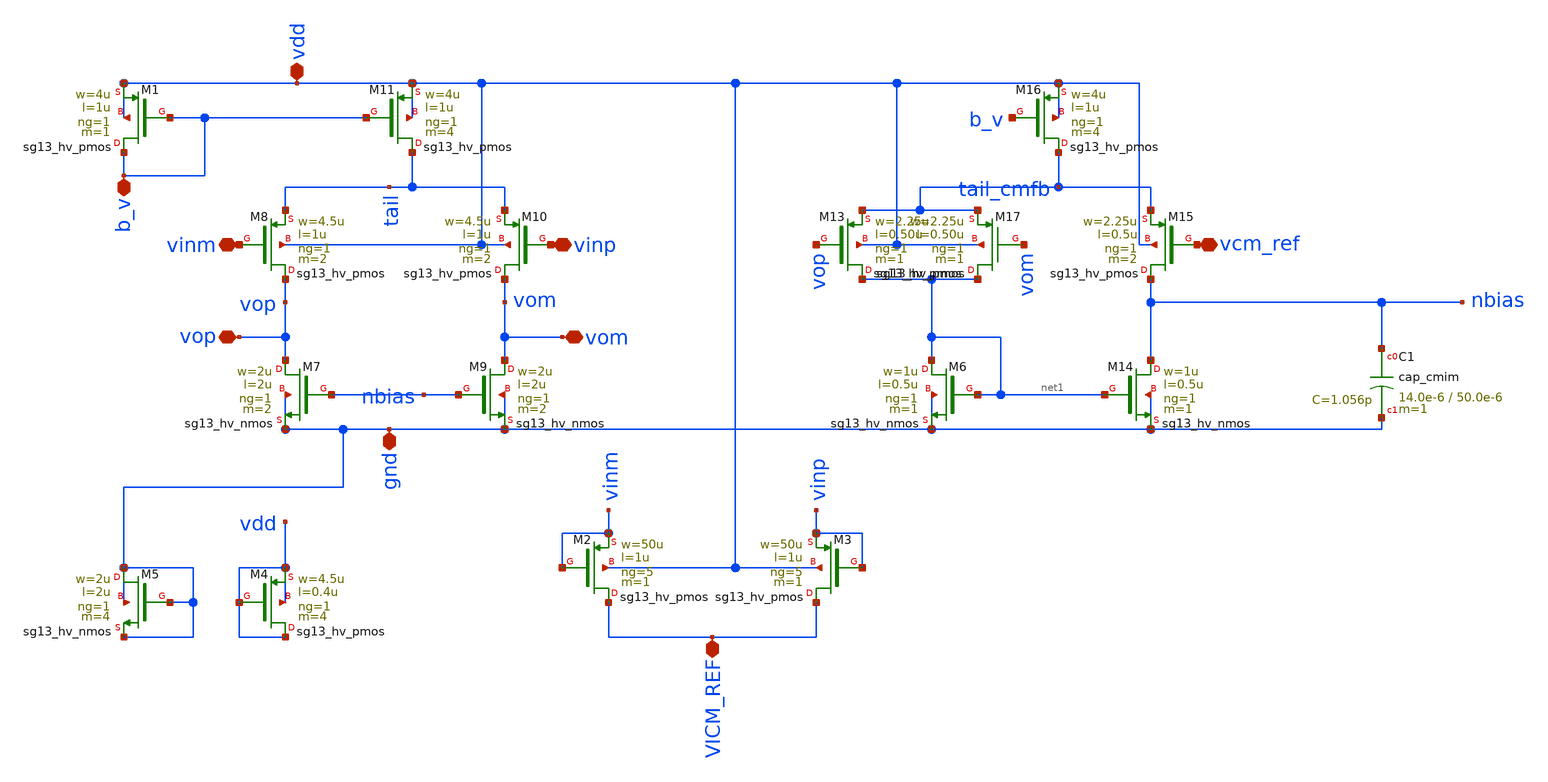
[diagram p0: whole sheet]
** sch_path: dependencies/OTA/OTA-main/schematic/xschem/Differntial_ended_symbol_making.sch
**.subckt Differntial_ended_symbol_making b_v vinm vcm_ref vinp vop vom gnd vdd VICM_REF
*.iopin b_v
*.iopin vinm
*.iopin vcm_ref
*.iopin vinp
*.iopin vop
*.iopin vom
*.iopin gnd
*.iopin vdd
*.iopin VICM_REF
XM7 vop nbias gnd gnd sg13_hv_nmos w=2u l=2u ng=1 m=2 mm_ok=1
XM8 vop vinm tail vdd sg13_hv_pmos w=4.5u l=1u ng=1 m=2 mm_ok=1
XM9 vom nbias gnd gnd sg13_hv_nmos w=2u l=2u ng=1 m=2 mm_ok=1
XM10 vom vinp tail vdd sg13_hv_pmos w=4.5u l=1u ng=1 m=2 mm_ok=1
XM11 tail b_v vdd vdd sg13_hv_pmos w=4u l=1u ng=1 m=4 mm_ok=1
XM6 net1 net1 gnd gnd sg13_hv_nmos w=1u l=0.5u ng=1 m=1 mm_ok=1
XM13 net1 vop tail_cmfb vdd sg13_hv_pmos w=2.25u l=0.50u ng=1 m=1 mm_ok=1
XM14 nbias net1 gnd gnd sg13_hv_nmos w=1u l=0.5u ng=1 m=1 mm_ok=1
XM15 nbias vcm_ref tail_cmfb vdd sg13_hv_pmos w=2.25u l=0.5u ng=1 m=2 mm_ok=1
XM16 tail_cmfb b_v vdd vdd sg13_hv_pmos w=4u l=1u ng=1 m=4 mm_ok=1
XM17 net1 vom tail_cmfb vdd sg13_hv_pmos w=2.25u l=0.50u ng=1 m=1 mm_ok=1
XM1 b_v b_v vdd vdd sg13_hv_pmos w=4u l=1u ng=1 m=1 mm_ok=1
XC1 nbias gnd cap_cmim w=14.0e-6 l=50.0e-6 m=1 mm_ok=1
XM2 VICM_REF vinm vinm vdd sg13_hv_pmos w=50u l=1u ng=5 m=1 mm_ok=1
XM3 VICM_REF vinp vinp vdd sg13_hv_pmos w=50u l=1u ng=5 m=1 mm_ok=1
XM4 vdd vdd vdd vdd sg13_hv_pmos w=4.5u l=0.4u ng=1 m=4 mm_ok=1
XM5 gnd gnd gnd gnd sg13_hv_nmos w=2u l=2u ng=1 m=4 mm_ok=1
**.ends
.end
